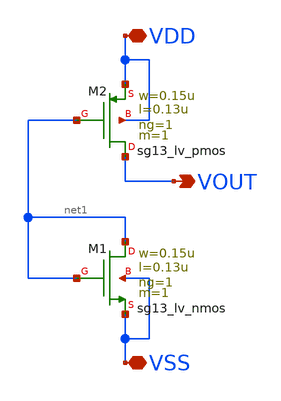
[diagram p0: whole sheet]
** sch_path: CDR4176-main/schematic/xschem/tieh_custom/tieh_custom.sch
**.subckt tieh_custom VDD VSS VOUT
*.iopin VDD
*.iopin VSS
*.opin VOUT
XM2 VOUT net1 VDD VDD sg13_lv_pmos w=0.15u l=0.13u ng=1 m=1 mm_ok=1
XM1 net1 net1 VSS VSS sg13_lv_nmos w=0.15u l=0.13u ng=1 m=1 mm_ok=1
**.ends
.end
